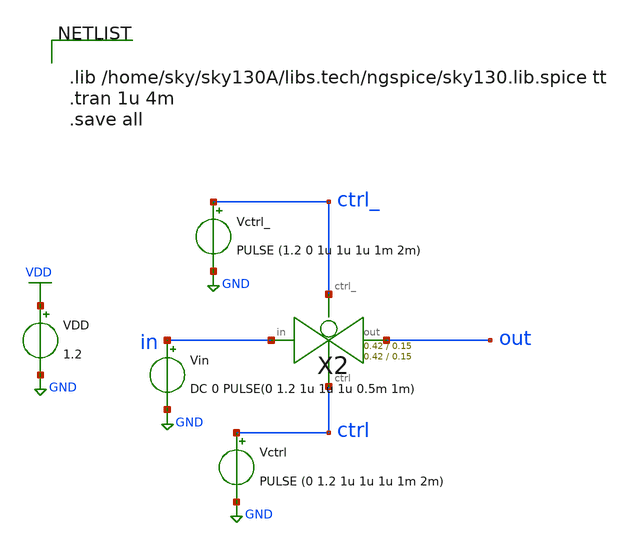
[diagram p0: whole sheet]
** sch_path: xschem/transmission_gate/transmission_gate_tb.sch
**.subckt transmission_gate_tb
Vin in GND DC 0 PULSE(0 1.2 1u 1u 1u 0.5m 1m)
VDD VDD GND 1.2
Vctrl ctrl GND PULSE (0 1.2 1u 1u 1u 1m 2m)
Vctrl_ ctrl_ GND PULSE (1.2 0 1u 1u 1u 1m 2m)
X2 in out ctrl_ ctrl transmission_gate Wpmos=0.42 Lpmos=0.15 Wnmos=0.42 Lnmos=0.15
**** begin user architecture code


.lib /home/sky/sky130A/libs.tech/ngspice/sky130.lib.spice tt
.tran 1u 4m
.save all


**** end user architecture code
**.ends

* expanding   symbol:  transmission_gate/transmission_gate.sym # of pins=4
** sym_path: xschem/transmission_gate/transmission_gate.sym
** sch_path: xschem/transmission_gate/transmission_gate.sch
.subckt transmission_gate in out ctrl_ ctrl  Wpmos=0.42 Lpmos=0.18 Wnmos=0.42 Lnmos=0.18
*.iopin in
*.iopin out
*.ipin ctrl_
*.ipin ctrl
XM1 out ctrl in GND sky130_fd_pr__nfet_01v8 L=Lnmos W=Wnmos nf=1 ad='int((nf+1)/2) * W/nf * 0.29' as='int((nf+2)/2) * W/nf * 0.29'
+ pd='2*int((nf+1)/2) * (W/nf + 0.29)' ps='2*int((nf+2)/2) * (W/nf + 0.29)' nrd='0.29 / W' nrs='0.29 / W'
+ sa=0 sb=0 sd=0 mult=1 m=1
XM2 out ctrl_ in VDD sky130_fd_pr__pfet_01v8 L=Lpmos W=Wpmos nf=1 ad='int((nf+1)/2) * W/nf * 0.29' as='int((nf+2)/2) * W/nf * 0.29'
+ pd='2*int((nf+1)/2) * (W/nf + 0.29)' ps='2*int((nf+2)/2) * (W/nf + 0.29)' nrd='0.29 / W' nrs='0.29 / W'
+ sa=0 sb=0 sd=0 mult=1 m=1
.ends

.GLOBAL VDD
.GLOBAL GND
.end
